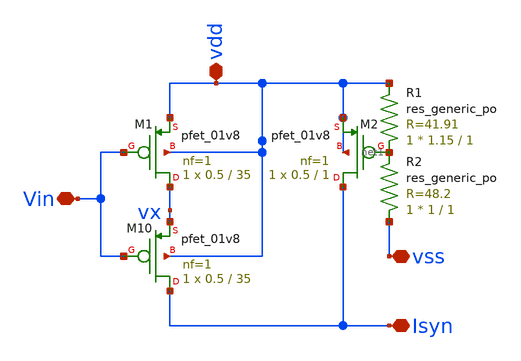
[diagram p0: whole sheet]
** sch_path: Neuron/ultralif/syn_neg.sch
**.subckt syn_neg Vin Isyn vdd vss
*.iopin Vin
*.iopin Isyn
*.iopin vdd
*.iopin vss
XM10 Isyn Vin vx vdd sky130_fd_pr__pfet_01v8 L=35 W=0.5 nf=1 ad='int((nf+1)/2) * W/nf * 0.29' as='int((nf+2)/2) * W/nf * 0.29'
+ pd='2*int((nf+1)/2) * (W/nf + 0.29)' ps='2*int((nf+2)/2) * (W/nf + 0.29)' nrd='0.29 / W' nrs='0.29 / W'
+ sa=0 sb=0 sd=0 mult=1 m=1
XM1 vx Vin vdd vdd sky130_fd_pr__pfet_01v8 L=35 W=0.5 nf=1 ad='int((nf+1)/2) * W/nf * 0.29' as='int((nf+2)/2) * W/nf * 0.29'
+ pd='2*int((nf+1)/2) * (W/nf + 0.29)' ps='2*int((nf+2)/2) * (W/nf + 0.29)' nrd='0.29 / W' nrs='0.29 / W'
+ sa=0 sb=0 sd=0 mult=1 m=1
XM2 Isyn net1 vdd vdd sky130_fd_pr__pfet_01v8 L=1 W=0.5 nf=1 ad='int((nf+1)/2) * W/nf * 0.29' as='int((nf+2)/2) * W/nf * 0.29'
+ pd='2*int((nf+1)/2) * (W/nf + 0.29)' ps='2*int((nf+2)/2) * (W/nf + 0.29)' nrd='0.29 / W' nrs='0.29 / W'
+ sa=0 sb=0 sd=0 mult=1 m=1
XR1 net1 vdd sky130_fd_pr__res_generic_po W=1.15 L=1 m=1
XR2 vss net1 sky130_fd_pr__res_generic_po W=1 L=1 m=1
**.ends
.end
